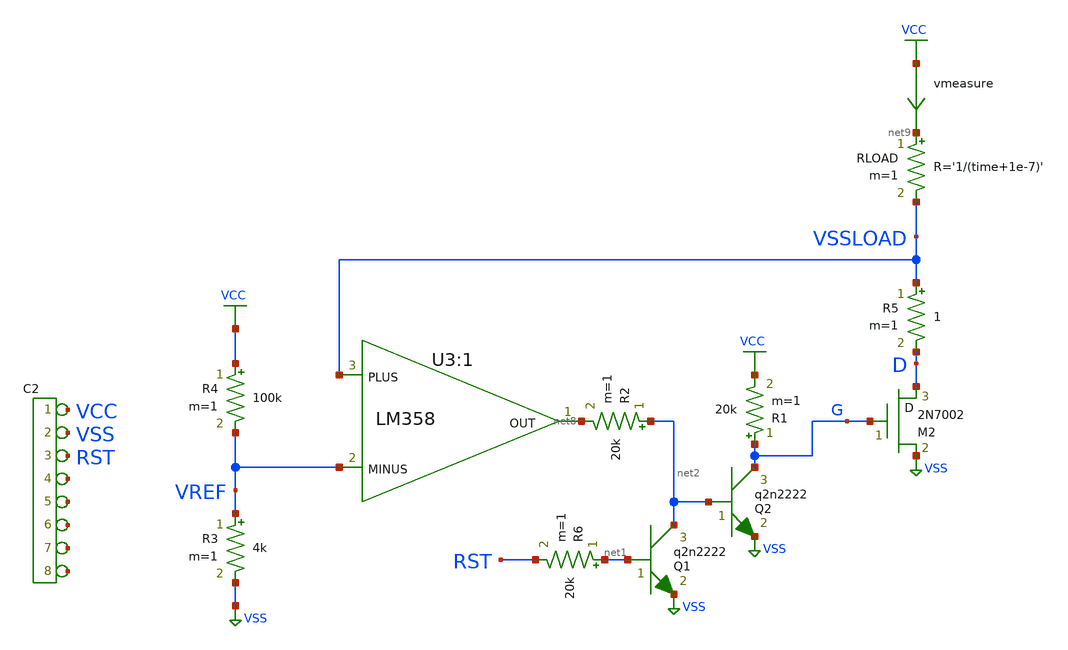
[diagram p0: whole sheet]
** sch_path: xschem_libraries_oa/pcb/pcb_current_protection_embed/schematic/pcb_current_protection_embed.sch
* Copyright (C) 1998-2024 Stefan Frederik Schippers
* This program is free software; you can redistribute it and/or modify
* it under the terms of the GNU General Public License as published by
* the Free Software Foundation; either version 2 of the License, or
* (at your option) any later version.
* This program is distributed in the hope that it will be useful,
* but WITHOUT ANY WARRANTY; without even the implied warranty of
* MERCHANTABILITY or FITNESS FOR A PARTICULAR PURPOSE.  See the
* GNU General Public License for more details.
* You should have received a copy of the GNU General Public License
* along with this program; if not, write to the Free Software
**.subckt pcb_current_protection_embed
*connector(8,1) ?1 VCC ?1 VSS ?1 RST ?1 net3 ?1 net4 ?1 net5 ?1 net6 ?1 net7
XU3:1 VSSLOAD VREF VCC VSS net8 LM358
R3 VREF VSS 4k m=1
R4 VCC VREF 100k m=1
XM2 D G VSS M2N7002 m=1
R5 VSSLOAD D 1 m=1
RLOAD net9 VSSLOAD R='1/(time+1e-7)' m=1
vmeasure VCC net9 0
.save i(vmeasure)
R2 net2 net8 20k m=1
Q1 net2 net1 VSS q2n2222 area=1 m=1
R6 net1 RST 20k m=1
Q2 G net2 VSS q2n2222 area=1 m=1
R1 G VCC 20k m=1
**** begin user architecture code


*.option PARHIER=LOCAL RUNLVL=5 post MODMONTE=1 warn maxwarns=400 ingold=1


vvcc vcc 0 dc 5
vvss vss 0 dc 0
vrst rst 0 pwl 0 5 100u 5 101u 0

** models are generally not free: you must download
** SPICE models for active devices and put them  into the below
** referenced file in netlist/simulation directory.
.include "models_pcb_current_protection.txt"
* .dc RLOAD 10K 1 -0.001
.control
  save all
  tran 10u 200m
  write pcb_current_protection_embed.raw
.endc


**** end user architecture code
**.ends
.GLOBAL VSS
.GLOBAL VCC
.end
